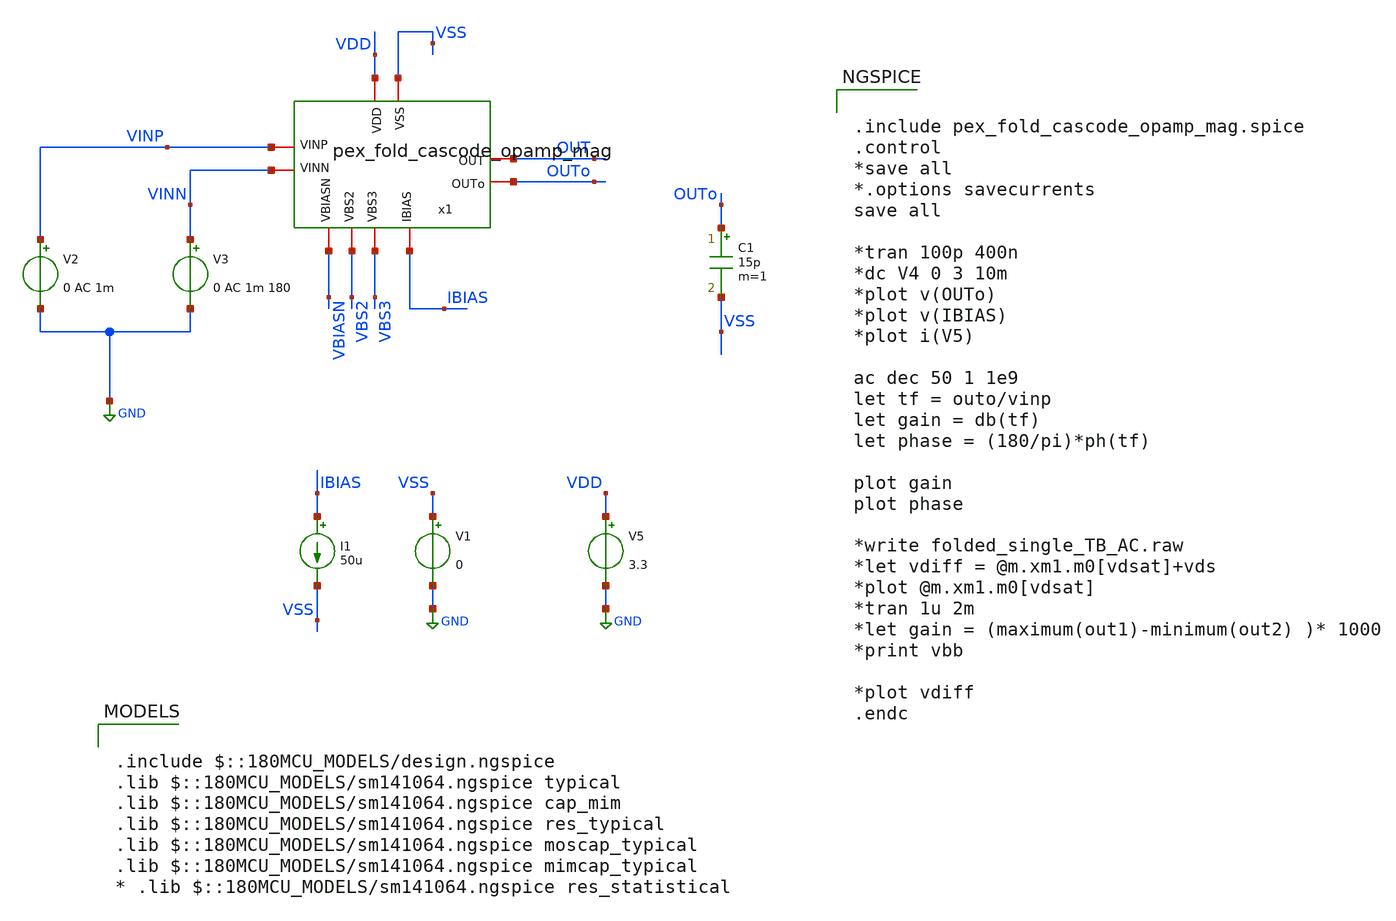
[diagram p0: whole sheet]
** sch_path: SCOP_INPUT_AND_MUX_PAKISTAN_03/Xschem/Folded_single/folded_single_TB_AC.sch
**.subckt folded_single_TB_AC
V5 VDD GND 3.3
V2 VINP GND 0 AC 1m
V1 VSS GND 0
I1 IBIAS VSS 50u
C1 OUTo VSS 15p m=1
V3 VINN GND 0 AC 1m 180
x1 OUT VDD VSS VINN VINP IBIAS VBS2 VBS3 VBIASN OUTo pex_fold_cascode_opamp_mag
**** begin user architecture code

.include $::180MCU_MODELS/design.ngspice
.lib $::180MCU_MODELS/sm141064.ngspice typical
.lib $::180MCU_MODELS/sm141064.ngspice cap_mim
.lib $::180MCU_MODELS/sm141064.ngspice res_typical
.lib $::180MCU_MODELS/sm141064.ngspice moscap_typical
.lib $::180MCU_MODELS/sm141064.ngspice mimcap_typical
* .lib $::180MCU_MODELS/sm141064.ngspice res_statistical



.include pex_fold_cascode_opamp_mag.spice
.control
*save all
*.options savecurrents
save all

*tran 100p 400n
*dc V4 0 3 10m
*plot v(OUTo)
*plot v(IBIAS)
*plot i(V5)

ac dec 50 1 1e9
let tf = outo/vinp
let gain = db(tf)
let phase = (180/pi)*ph(tf)

plot gain
plot phase

*write folded_single_TB_AC.raw
*let vdiff = @m.xm1.m0[vdsat]+vds
*plot @m.xm1.m0[vdsat]
*tran 1u 2m
*let gain = (maximum(out1)-minimum(out2) )* 1000
*print vbb

*plot vdiff
.endc


**** end user architecture code
**.ends
.GLOBAL GND
.end
